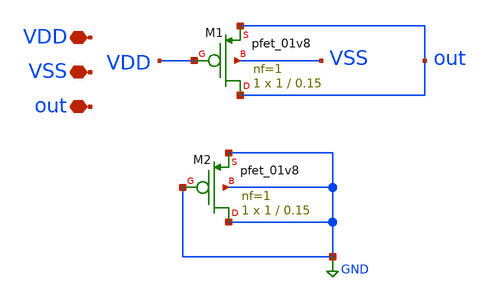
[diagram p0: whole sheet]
** sch_path: xschem/shorted_test.sch
**.subckt shorted_test VSS out VDD
*.iopin VSS
*.iopin out
*.iopin VDD
XM1 out VDD out VSS sky130_fd_pr__pfet_01v8 L=0.15 W=1 nf=1 ad='int((nf+1)/2) * W/nf * 0.29' as='int((nf+2)/2) * W/nf * 0.29'
+ pd='2*int((nf+1)/2) * (W/nf + 0.29)' ps='2*int((nf+2)/2) * (W/nf + 0.29)' nrd='0.29 / W' nrs='0.29 / W'
+ sa=0 sb=0 sd=0 mult=1 m=1
XM2 GND GND GND GND sky130_fd_pr__pfet_01v8 L=0.15 W=1 nf=1 ad='int((nf+1)/2) * W/nf * 0.29' as='int((nf+2)/2) * W/nf * 0.29'
+ pd='2*int((nf+1)/2) * (W/nf + 0.29)' ps='2*int((nf+2)/2) * (W/nf + 0.29)' nrd='0.29 / W' nrs='0.29 / W'
+ sa=0 sb=0 sd=0 mult=1 m=1
**.ends
.GLOBAL GND
.end
